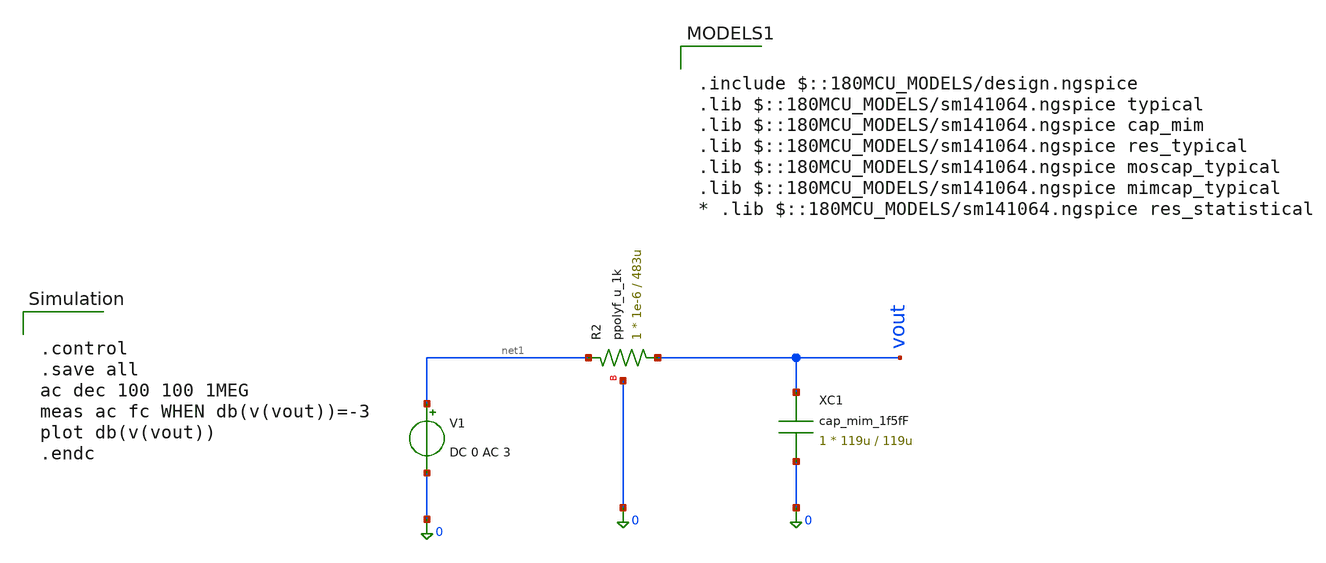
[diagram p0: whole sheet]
** sch_path: designs/libs/tb_analog/tb_lpf/tb_lpf.sch
**.subckt tb_lpf
XC1 vout 0 cap_mim_1f5fF c_width=119u c_length=119u m=1
XR2 vout net1 0 ppolyf_u_1k r_width=1e-6 r_length=483u m=1
V1 net1 0 DC 0 AC 3
**** begin user architecture code


.control
.save all
ac dec 100 100 1MEG
meas ac fc WHEN db(v(vout))=-3
plot db(v(vout))
.endc



.include $::180MCU_MODELS/design.ngspice
.lib $::180MCU_MODELS/sm141064.ngspice typical
.lib $::180MCU_MODELS/sm141064.ngspice cap_mim
.lib $::180MCU_MODELS/sm141064.ngspice res_typical
.lib $::180MCU_MODELS/sm141064.ngspice moscap_typical
.lib $::180MCU_MODELS/sm141064.ngspice mimcap_typical
* .lib $::180MCU_MODELS/sm141064.ngspice res_statistical

**** end user architecture code
**.ends
.end
